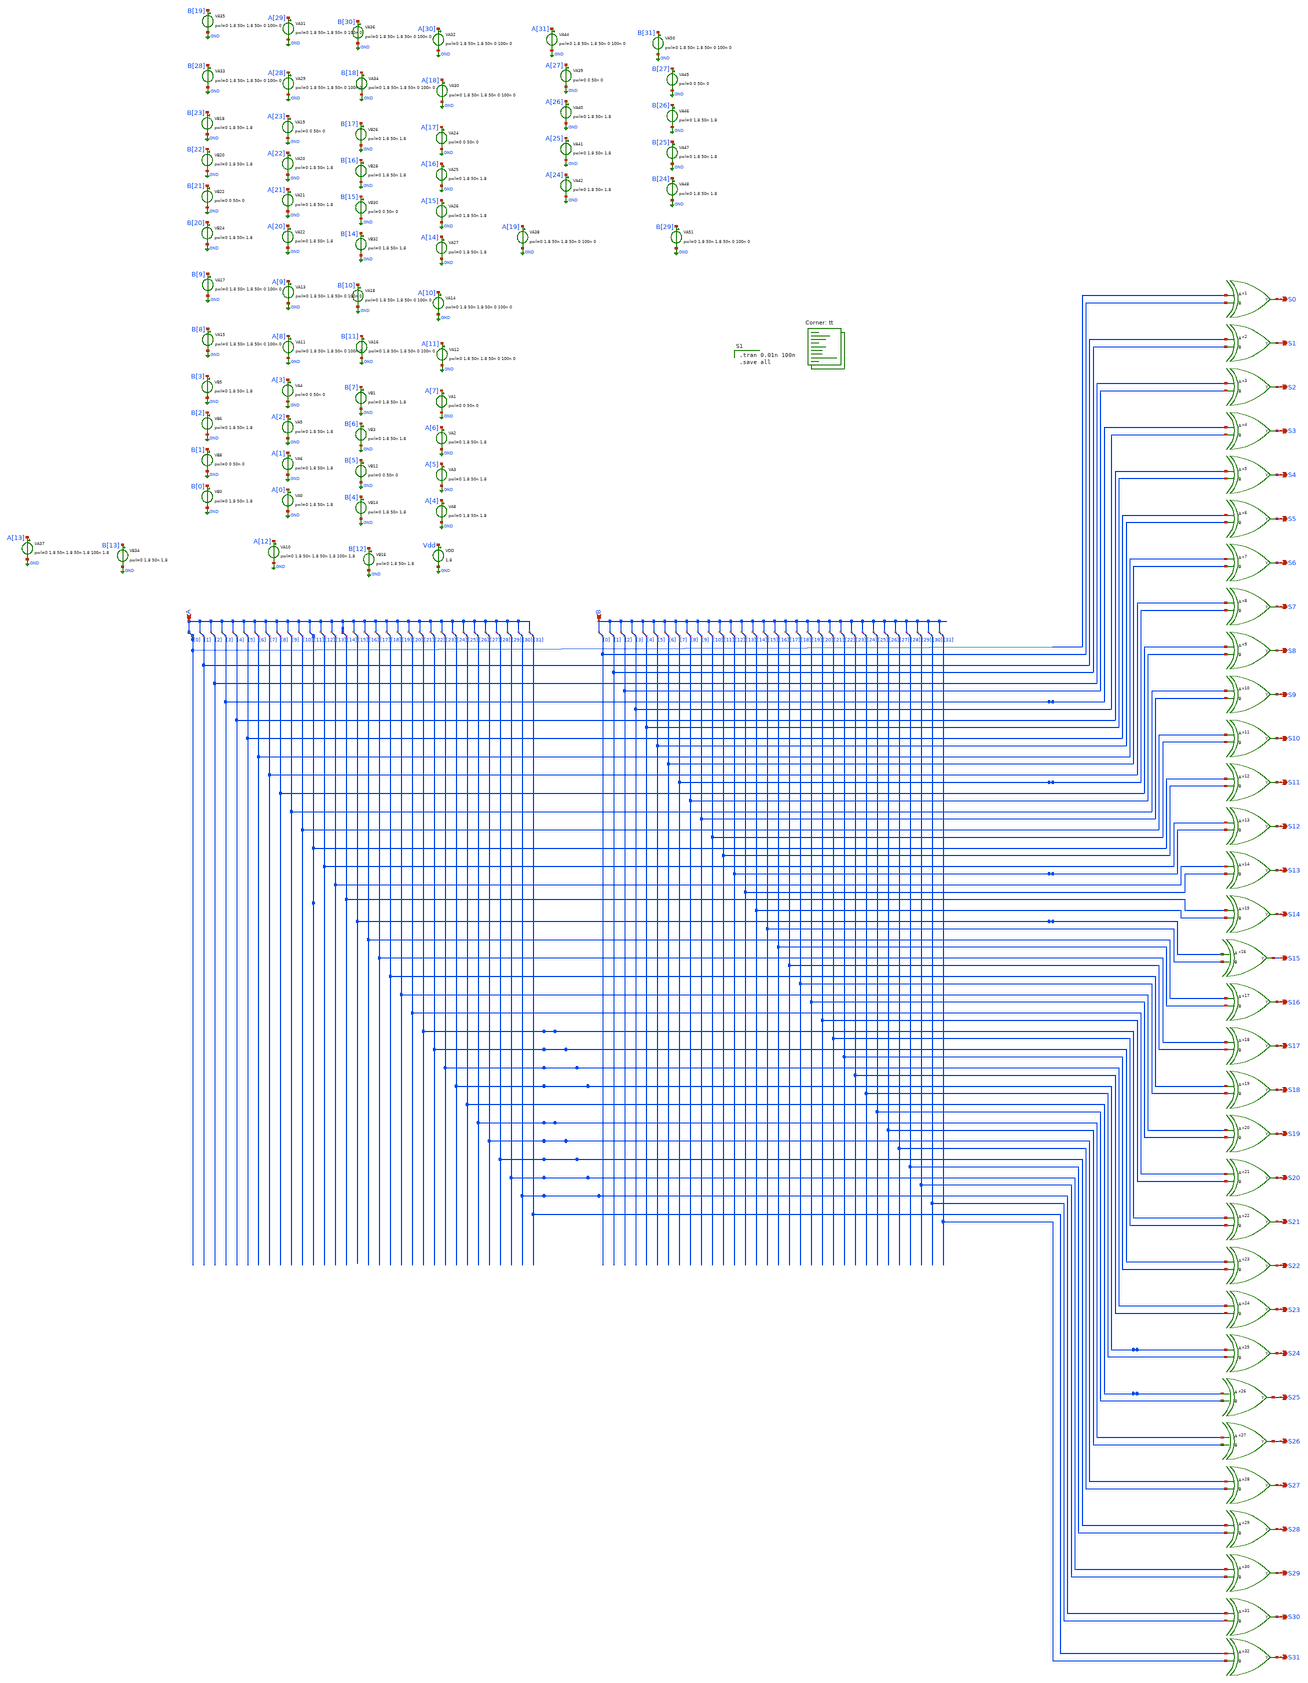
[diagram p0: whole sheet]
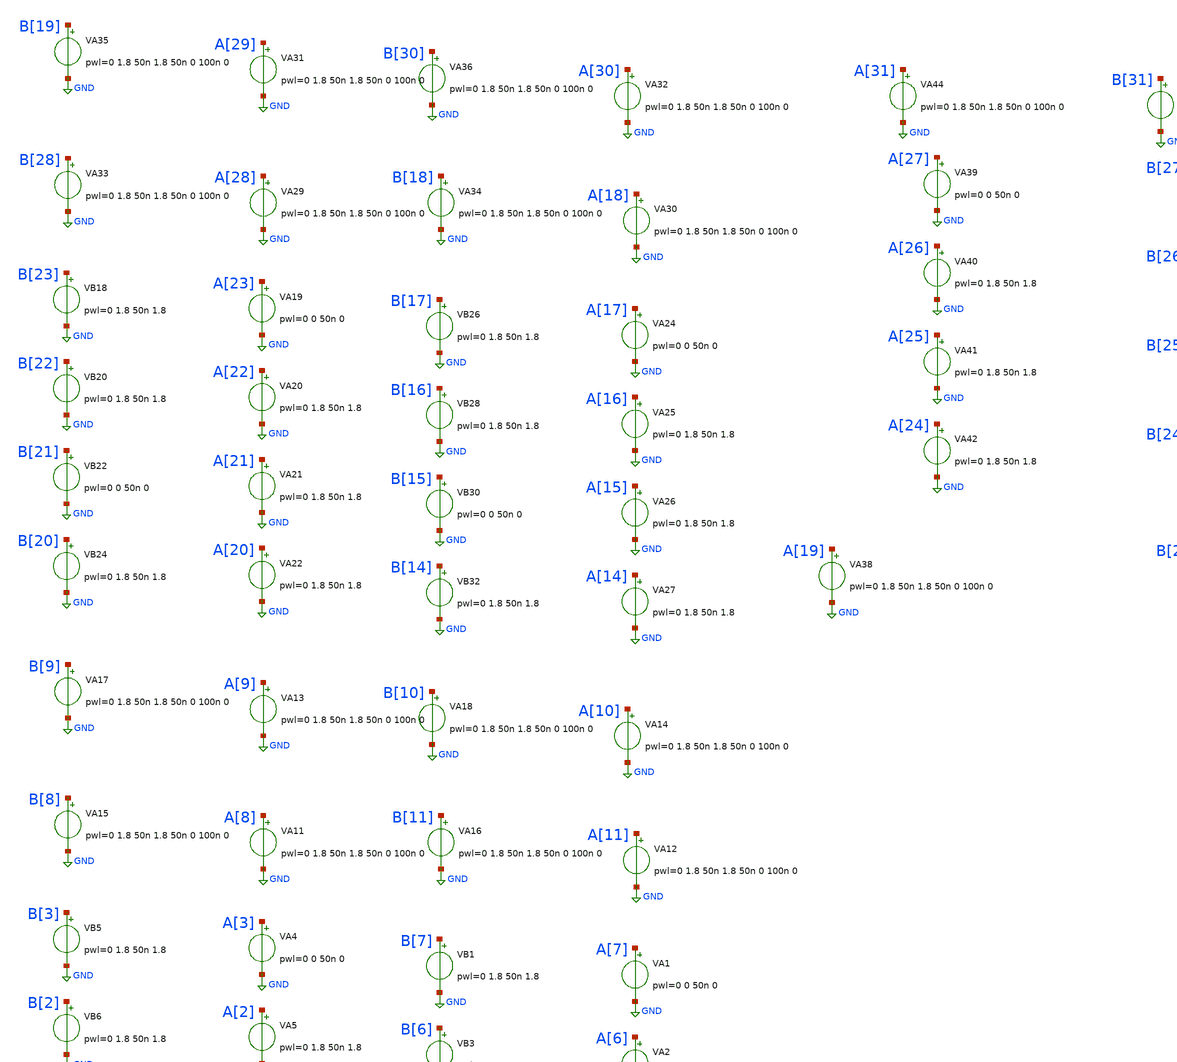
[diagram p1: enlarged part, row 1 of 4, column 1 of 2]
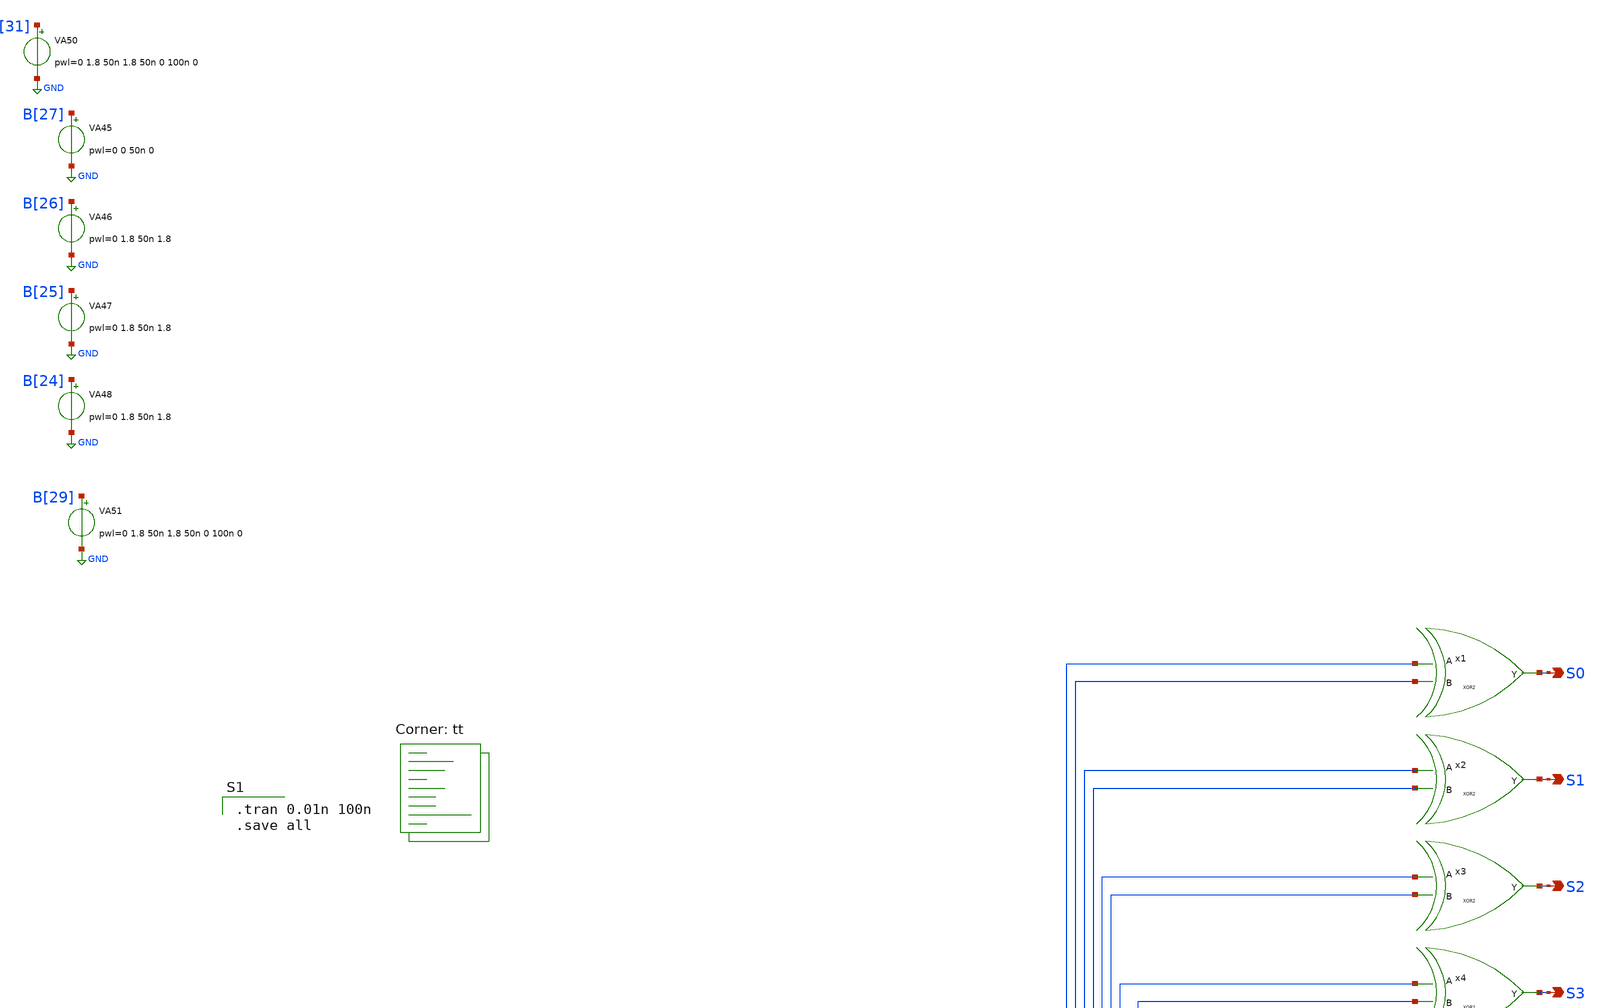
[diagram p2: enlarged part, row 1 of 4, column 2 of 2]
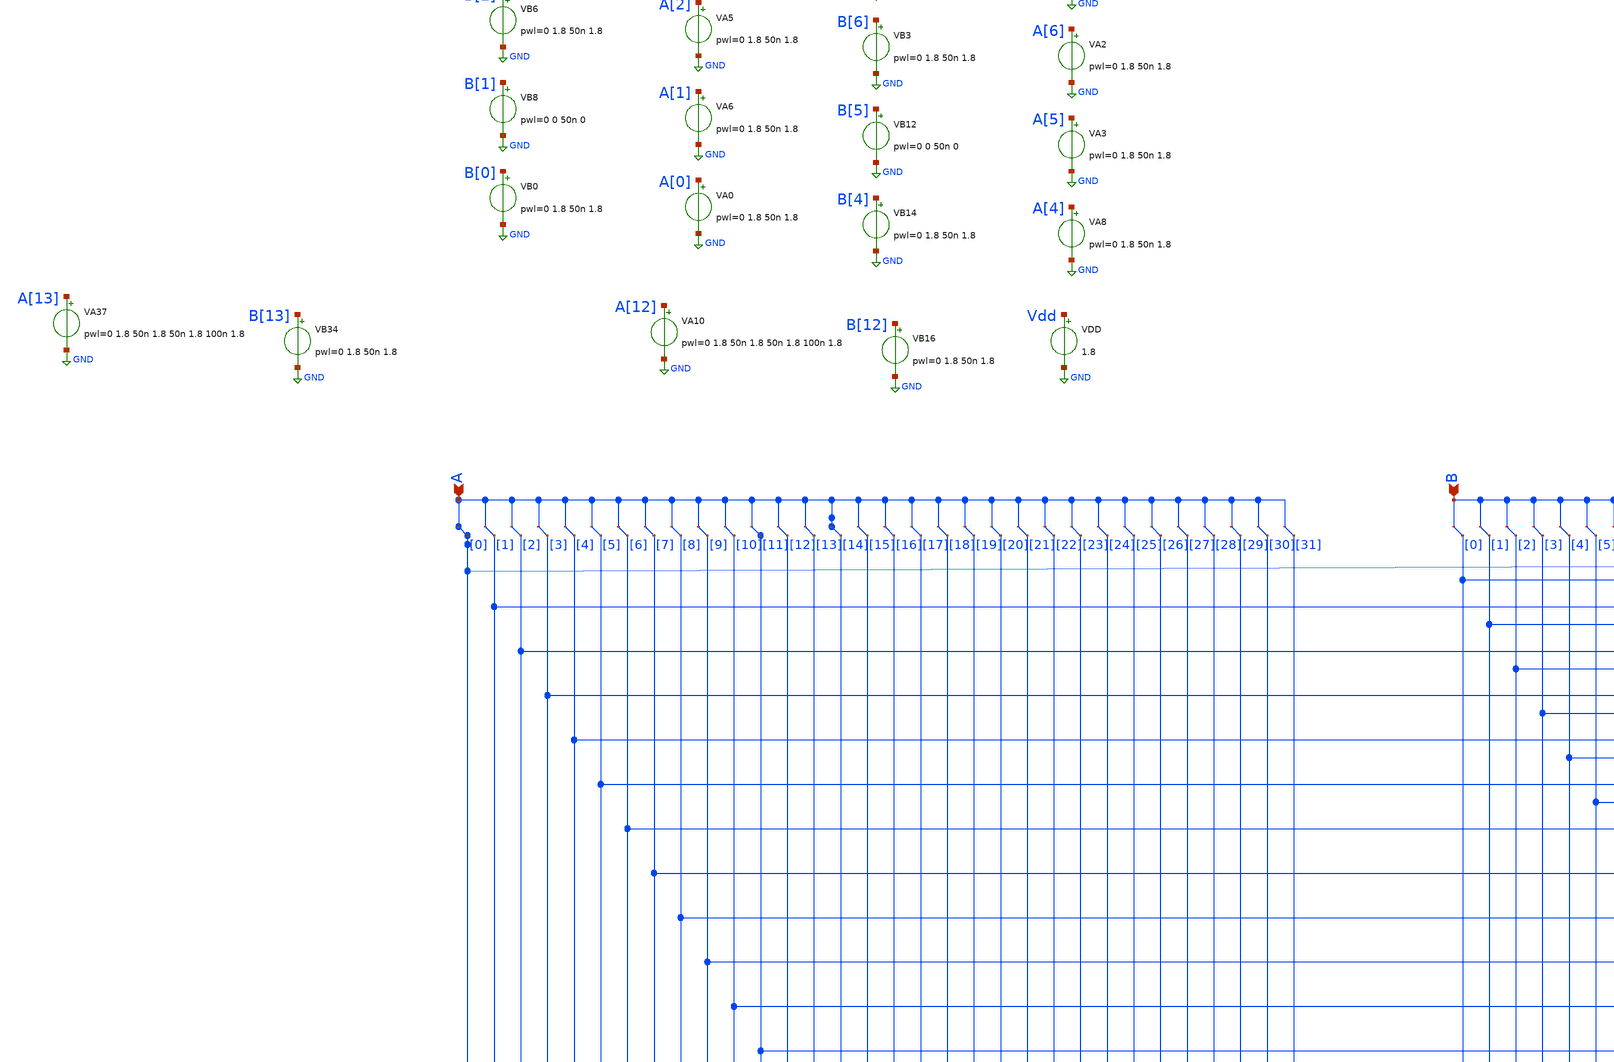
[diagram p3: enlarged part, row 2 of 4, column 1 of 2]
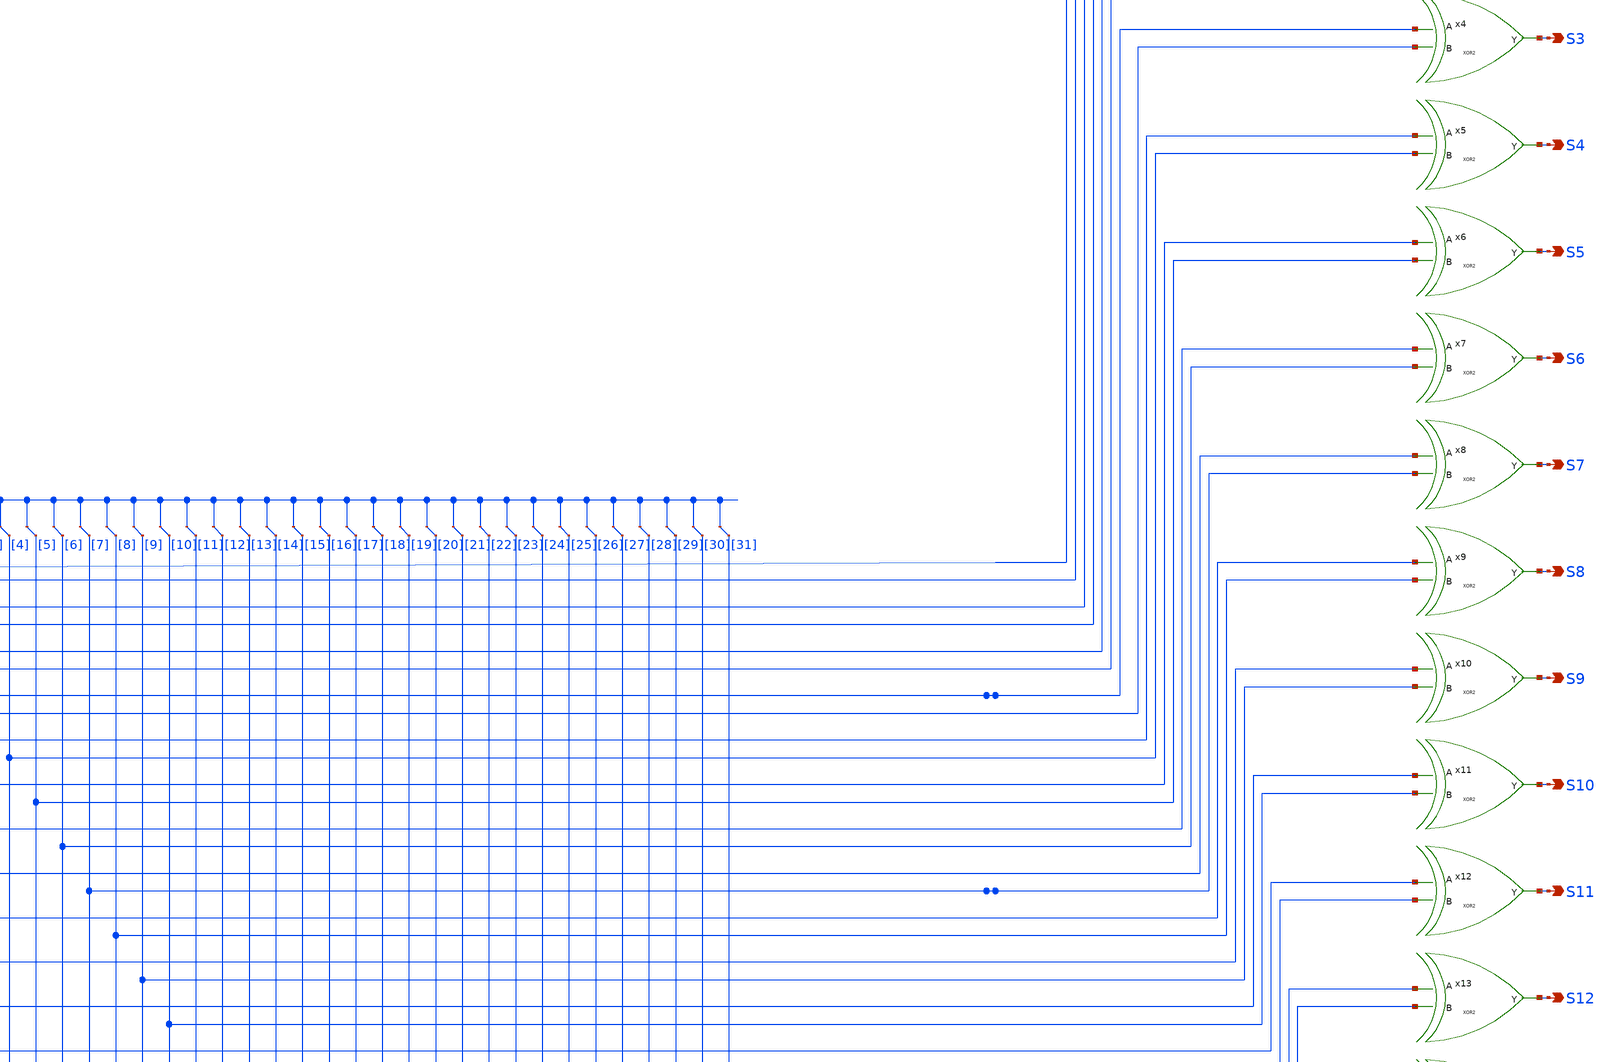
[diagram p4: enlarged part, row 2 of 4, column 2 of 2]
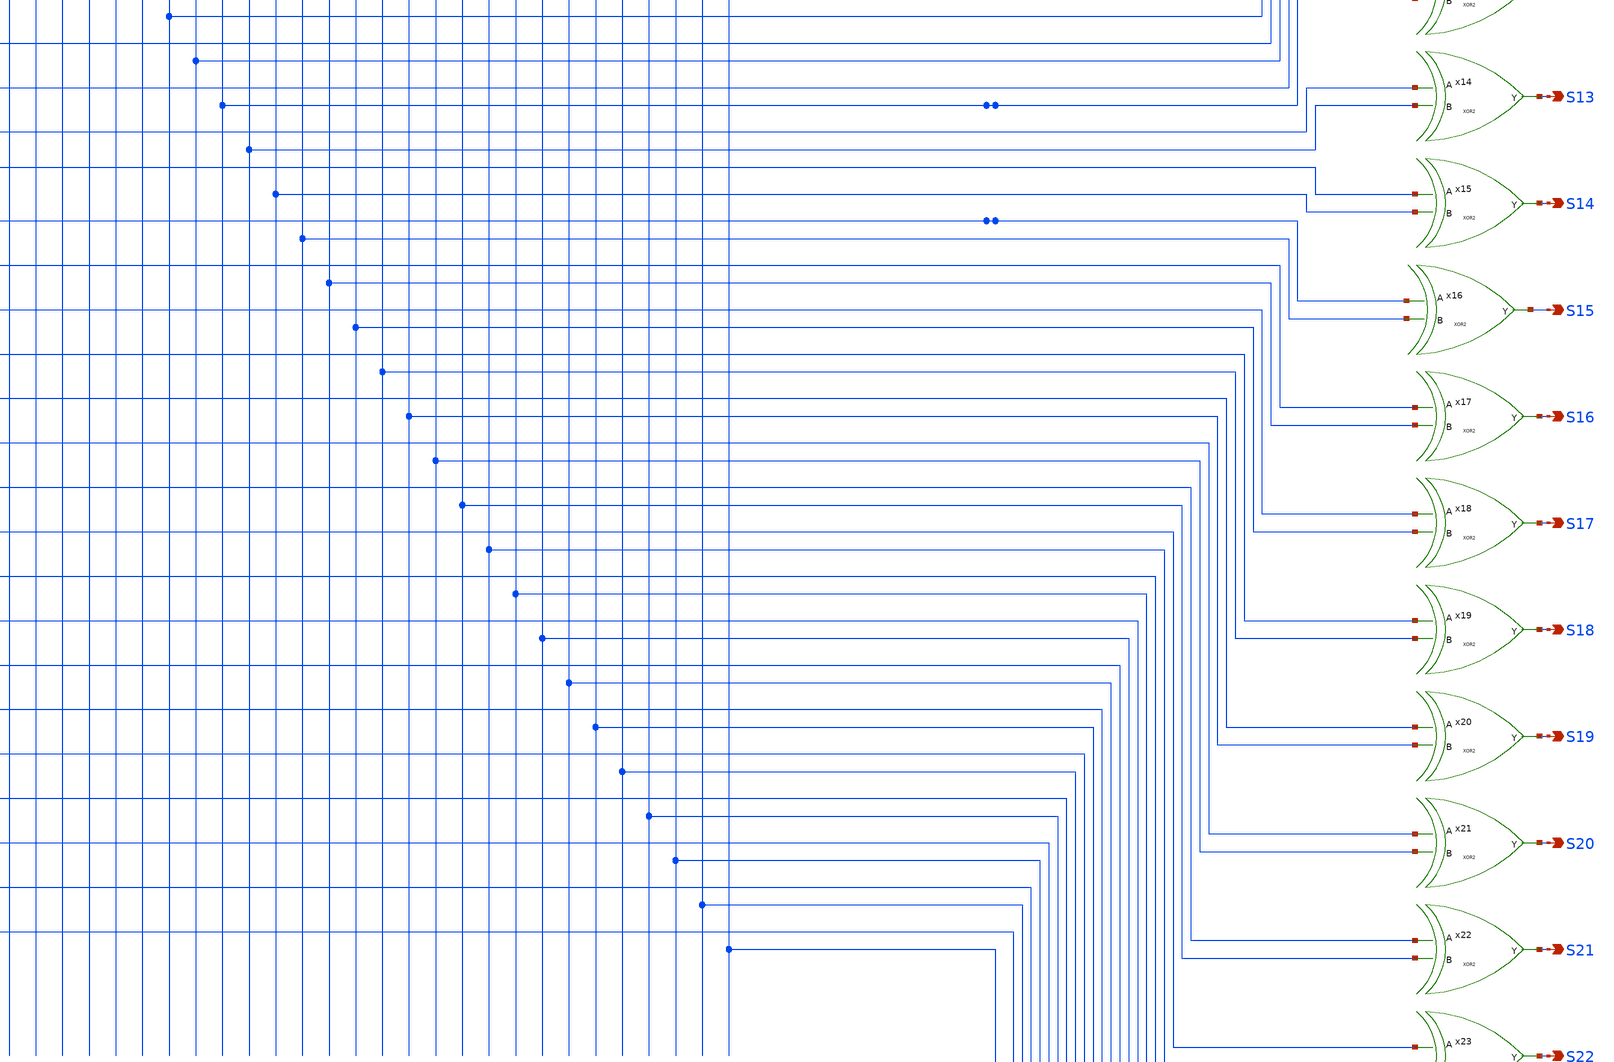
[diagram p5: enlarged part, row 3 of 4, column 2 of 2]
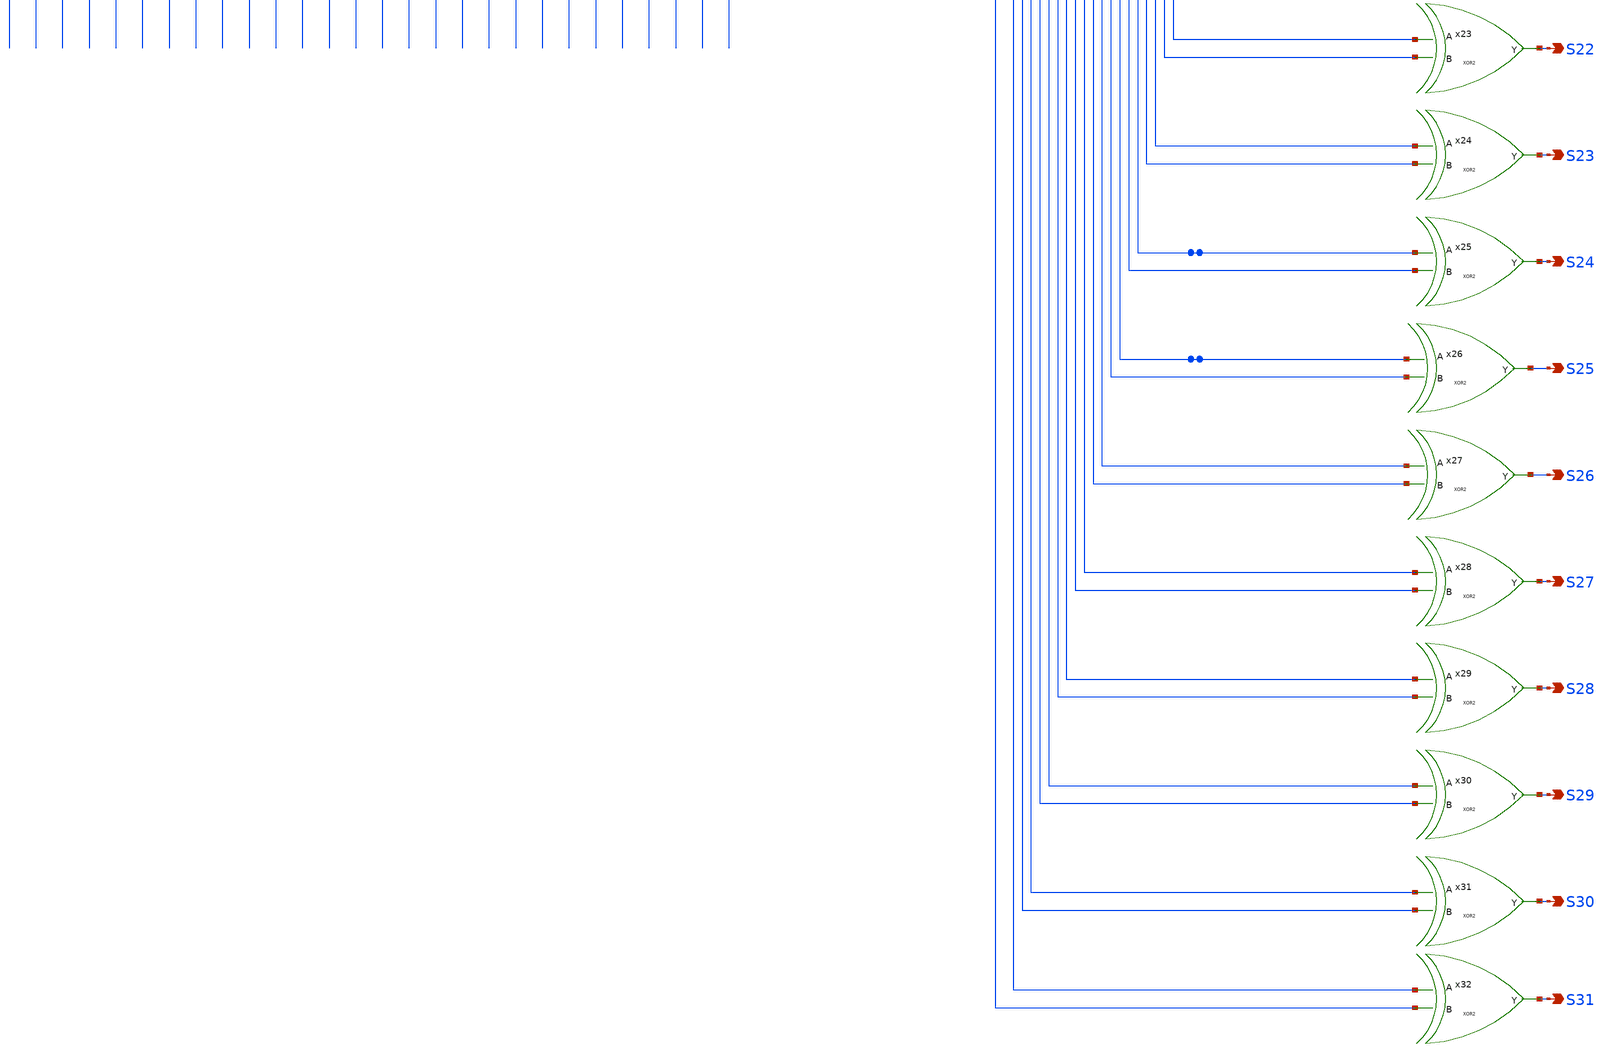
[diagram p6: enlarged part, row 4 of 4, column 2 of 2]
** sch_path: gates/32bit_XORsim.sch
**.subckt 32bit_XORsim S4 S5 S6 S7 S8 S9 S10 S11 S12 S13 S14 S15 S16 S17 S18 S19 S20 S21 S22 S23 S24
*+ S25 S26 S27 S28 S29 S30 S31 S0 S1 S2 S3 A B
*.opin S4
*.opin S5
*.opin S6
*.opin S7
*.opin S8
*.opin S9
*.opin S10
*.opin S11
*.opin S12
*.opin S13
*.opin S14
*.opin S15
*.opin S16
*.opin S17
*.opin S18
*.opin S19
*.opin S20
*.opin S21
*.opin S22
*.opin S23
*.opin S24
*.opin S25
*.opin S26
*.opin S27
*.opin S28
*.opin S29
*.opin S30
*.opin S31
*.opin S0
*.opin S1
*.opin S2
*.opin S3
*.ipin A
*.ipin B
* tap: A --> A[0]
* tap: A --> A[1]
* tap: A --> A[2]
* tap: A --> A[3]
* tap: A --> A[4]
* tap: A --> A[5]
* tap: A --> A[6]
* tap: A --> A[7]
* tap: A --> A[8]
* tap: A --> A[9]
* tap: A --> A[10]
* tap: A --> A[11]
* tap: A --> A[12]
* tap: A --> A[13]
* tap: A --> A[14]
* tap: A --> A[15]
* tap: A --> A[16]
* tap: A --> A[17]
* tap: A --> A[18]
* tap: A --> A[19]
* tap: A --> A[20]
* tap: A --> A[21]
* tap: A --> A[22]
* tap: A --> A[23]
* tap: A --> A[24]
* tap: A --> A[25]
* tap: A --> A[26]
* tap: A --> A[27]
* tap: A --> A[28]
* tap: A --> A[29]
* tap: A --> A[30]
* tap: A --> A[31]
* tap: B --> B[0]
* tap: B --> B[1]
* tap: B --> B[2]
* tap: B --> B[3]
* tap: B --> B[4]
* tap: B --> B[5]
* tap: B --> B[6]
* tap: B --> B[7]
* tap: B --> B[8]
* tap: B --> B[9]
* tap: B --> B[10]
* tap: B --> B[11]
* tap: B --> B[12]
* tap: B --> B[13]
* tap: B --> B[14]
* tap: B --> B[15]
* tap: B --> B[16]
* tap: B --> B[17]
* tap: B --> B[18]
* tap: B --> B[19]
* tap: B --> B[20]
* tap: B --> B[21]
* tap: B --> B[22]
* tap: B --> B[23]
* tap: B --> B[24]
* tap: B --> B[25]
* tap: B --> B[26]
* tap: B --> B[27]
* tap: B --> B[28]
* tap: B --> B[29]
* tap: B --> B[30]
* tap: B --> B[31]
VA10 A[12] GND pwl=0 1.8 50n 1.8 50n 1.8 100n 1.8
VB16 B[12] GND pwl=0 1.8 50n 1.8
VDD Vdd GND 1.8
VA4 A[3] GND pwl=0 0 50n 0
VA5 A[2] GND pwl=0 1.8 50n 1.8
VA6 A[1] GND pwl=0 1.8 50n 1.8
VA0 A[0] GND pwl=0 1.8 50n 1.8
VB5 B[3] GND pwl=0 1.8 50n 1.8
VB6 B[2] GND pwl=0 1.8 50n 1.8
VB8 B[1] GND pwl=0 0 50n 0
VB0 B[0] GND pwl=0 1.8 50n 1.8
VA1 A[7] GND pwl=0 0 50n 0
VA2 A[6] GND pwl=0 1.8 50n 1.8
VA3 A[5] GND pwl=0 1.8 50n 1.8
VA8 A[4] GND pwl=0 1.8 50n 1.8
VB1 B[7] GND pwl=0 1.8 50n 1.8
VB3 B[6] GND pwl=0 1.8 50n 1.8
VB12 B[5] GND pwl=0 0 50n 0
VB14 B[4] GND pwl=0 1.8 50n 1.8
VA11 A[8] GND pwl=0 1.8 50n 1.8 50n 0 100n 0
VA12 A[11] GND pwl=0 1.8 50n 1.8 50n 0 100n 0
VA13 A[9] GND pwl=0 1.8 50n 1.8 50n 0 100n 0
VA14 A[10] GND pwl=0 1.8 50n 1.8 50n 0 100n 0
VA15 B[8] GND pwl=0 1.8 50n 1.8 50n 0 100n 0
VA16 B[11] GND pwl=0 1.8 50n 1.8 50n 0 100n 0
VA17 B[9] GND pwl=0 1.8 50n 1.8 50n 0 100n 0
VA18 B[10] GND pwl=0 1.8 50n 1.8 50n 0 100n 0
VA19 A[23] GND pwl=0 0 50n 0
VA20 A[22] GND pwl=0 1.8 50n 1.8
VA21 A[21] GND pwl=0 1.8 50n 1.8
VA22 A[20] GND pwl=0 1.8 50n 1.8
VB18 B[23] GND pwl=0 1.8 50n 1.8
VB20 B[22] GND pwl=0 1.8 50n 1.8
VB22 B[21] GND pwl=0 0 50n 0
VB24 B[20] GND pwl=0 1.8 50n 1.8
VA24 A[17] GND pwl=0 0 50n 0
VA25 A[16] GND pwl=0 1.8 50n 1.8
VA26 A[15] GND pwl=0 1.8 50n 1.8
VA27 A[14] GND pwl=0 1.8 50n 1.8
VB26 B[17] GND pwl=0 1.8 50n 1.8
VB28 B[16] GND pwl=0 1.8 50n 1.8
VB30 B[15] GND pwl=0 0 50n 0
VB32 B[14] GND pwl=0 1.8 50n 1.8
VA29 A[28] GND pwl=0 1.8 50n 1.8 50n 0 100n 0
VA30 A[18] GND pwl=0 1.8 50n 1.8 50n 0 100n 0
VA31 A[29] GND pwl=0 1.8 50n 1.8 50n 0 100n 0
VA32 A[30] GND pwl=0 1.8 50n 1.8 50n 0 100n 0
VA33 B[28] GND pwl=0 1.8 50n 1.8 50n 0 100n 0
VA34 B[18] GND pwl=0 1.8 50n 1.8 50n 0 100n 0
VA35 B[19] GND pwl=0 1.8 50n 1.8 50n 0 100n 0
VA36 B[30] GND pwl=0 1.8 50n 1.8 50n 0 100n 0
VA37 A[13] GND pwl=0 1.8 50n 1.8 50n 1.8 100n 1.8
VB34 B[13] GND pwl=0 1.8 50n 1.8
VA38 A[19] GND pwl=0 1.8 50n 1.8 50n 0 100n 0
VA39 A[27] GND pwl=0 0 50n 0
VA40 A[26] GND pwl=0 1.8 50n 1.8
VA41 A[25] GND pwl=0 1.8 50n 1.8
VA42 A[24] GND pwl=0 1.8 50n 1.8
VA44 A[31] GND pwl=0 1.8 50n 1.8 50n 0 100n 0
VA45 B[27] GND pwl=0 0 50n 0
VA46 B[26] GND pwl=0 1.8 50n 1.8
VA47 B[25] GND pwl=0 1.8 50n 1.8
VA48 B[24] GND pwl=0 1.8 50n 1.8
VA50 B[31] GND pwl=0 1.8 50n 1.8 50n 0 100n 0
VA51 B[29] GND pwl=0 1.8 50n 1.8 50n 0 100n 0
x1 A[0] B[0] S0 XOR2
x2 A[1] B[1] S1 XOR2
x3 A[2] B[2] S2 XOR2
x4 A[3] B[3] S3 XOR2
x5 A[4] B[4] S4 XOR2
x6 A[5] B[5] S5 XOR2
x7 A[6] B[6] S6 XOR2
x8 A[7] B[7] S7 XOR2
x9 A[8] B[8] S8 XOR2
x10 A[9] B[9] S9 XOR2
x11 A[10] B[10] S10 XOR2
x12 A[11] B[11] S11 XOR2
x13 A[12] B[12] S12 XOR2
x14 A[13] B[13] S13 XOR2
x15 A[14] B[14] S14 XOR2
x16 A[15] B[15] S15 XOR2
x17 A[16] B[16] S16 XOR2
x18 A[17] B[17] S17 XOR2
x19 A[18] B[18] S18 XOR2
x20 A[19] B[19] S19 XOR2
x21 A[20] B[20] S20 XOR2
x22 A[21] B[21] S21 XOR2
x23 A[22] B[22] S22 XOR2
x24 A[23] B[23] S23 XOR2
x25 A[24] B[24] S24 XOR2
x26 A[25] B[25] S25 XOR2
x27 A[26] B[26] S26 XOR2
x28 A[27] B[27] S27 XOR2
x29 A[28] B[28] S28 XOR2
x30 A[29] B[29] S29 XOR2
x31 A[30] B[30] S30 XOR2
x32 A[31] B[31] S31 XOR2
**** begin user architecture code

.tran 0.01n 100n
.save all

.lib $::SKYWATER_MODELS/sky130.lib.spice tt
**** end user architecture code
**.ends

* expanding   symbol:  XOR2.sym # of pins=3
** sym_path: gates/XOR2.sym
** sch_path: gates/XOR2.sch
.subckt XOR2 B A Y
*.ipin A
*.ipin B
*.opin Y
XM1 Y A net5 GND sky130_fd_pr__nfet_01v8 L=0.15 W=1 nf=1 ad='int((nf+1)/2) * W/nf * 0.29' as='int((nf+2)/2) * W/nf * 0.29'
+ pd='2*int((nf+1)/2) * (W/nf + 0.29)' ps='2*int((nf+2)/2) * (W/nf + 0.29)' nrd='0.29 / W' nrs='0.29 / W'
+ sa=0 sb=0 sd=0 mult=1 m=1
XM2 net5 B GND GND sky130_fd_pr__nfet_01v8 L=0.15 W=1 nf=1 ad='int((nf+1)/2) * W/nf * 0.29' as='int((nf+2)/2) * W/nf * 0.29'
+ pd='2*int((nf+1)/2) * (W/nf + 0.29)' ps='2*int((nf+2)/2) * (W/nf + 0.29)' nrd='0.29 / W' nrs='0.29 / W'
+ sa=0 sb=0 sd=0 mult=1 m=1
XM3 Y net1 net2 VDD sky130_fd_pr__pfet_01v8 L=0.15 W=1 nf=1 ad='int((nf+1)/2) * W/nf * 0.29' as='int((nf+2)/2) * W/nf * 0.29'
+ pd='2*int((nf+1)/2) * (W/nf + 0.29)' ps='2*int((nf+2)/2) * (W/nf + 0.29)' nrd='0.29 / W' nrs='0.29 / W'
+ sa=0 sb=0 sd=0 mult=1 m=1
XM4 net2 A VDD VDD sky130_fd_pr__pfet_01v8 L=0.15 W=1 nf=1 ad='int((nf+1)/2) * W/nf * 0.29' as='int((nf+2)/2) * W/nf * 0.29'
+ pd='2*int((nf+1)/2) * (W/nf + 0.29)' ps='2*int((nf+2)/2) * (W/nf + 0.29)' nrd='0.29 / W' nrs='0.29 / W'
+ sa=0 sb=0 sd=0 mult=1 m=1
XM5 net2 B VDD VDD sky130_fd_pr__pfet_01v8 L=0.15 W=1 nf=1 ad='int((nf+1)/2) * W/nf * 0.29' as='int((nf+2)/2) * W/nf * 0.29'
+ pd='2*int((nf+1)/2) * (W/nf + 0.29)' ps='2*int((nf+2)/2) * (W/nf + 0.29)' nrd='0.29 / W' nrs='0.29 / W'
+ sa=0 sb=0 sd=0 mult=1 m=1
XM6 Y net3 net2 VDD sky130_fd_pr__pfet_01v8 L=0.15 W=1 nf=1 ad='int((nf+1)/2) * W/nf * 0.29' as='int((nf+2)/2) * W/nf * 0.29'
+ pd='2*int((nf+1)/2) * (W/nf + 0.29)' ps='2*int((nf+2)/2) * (W/nf + 0.29)' nrd='0.29 / W' nrs='0.29 / W'
+ sa=0 sb=0 sd=0 mult=1 m=1
XM7 Y net1 net4 GND sky130_fd_pr__nfet_01v8 L=0.15 W=1 nf=1 ad='int((nf+1)/2) * W/nf * 0.29' as='int((nf+2)/2) * W/nf * 0.29'
+ pd='2*int((nf+1)/2) * (W/nf + 0.29)' ps='2*int((nf+2)/2) * (W/nf + 0.29)' nrd='0.29 / W' nrs='0.29 / W'
+ sa=0 sb=0 sd=0 mult=1 m=1
XM8 net4 net3 GND GND sky130_fd_pr__nfet_01v8 L=0.15 W=1 nf=1 ad='int((nf+1)/2) * W/nf * 0.29' as='int((nf+2)/2) * W/nf * 0.29'
+ pd='2*int((nf+1)/2) * (W/nf + 0.29)' ps='2*int((nf+2)/2) * (W/nf + 0.29)' nrd='0.29 / W' nrs='0.29 / W'
+ sa=0 sb=0 sd=0 mult=1 m=1
X1 A net1 inv_vtc
X2 B net3 inv_vtc
.ends


* expanding   symbol:  inv_vtc.sym # of pins=2
** sym_path: gates/inv_vtc.sym
** sch_path: gates/inv_vtc.sch
.subckt inv_vtc A Y
*.ipin A
*.opin Y
XM1 Y A VDD VDD sky130_fd_pr__pfet_01v8 L=0.15 W=2 nf=1 ad='int((nf+1)/2) * W/nf * 0.29' as='int((nf+2)/2) * W/nf * 0.29'
+ pd='2*int((nf+1)/2) * (W/nf + 0.29)' ps='2*int((nf+2)/2) * (W/nf + 0.29)' nrd='0.29 / W' nrs='0.29 / W'
+ sa=0 sb=0 sd=0 mult=1 m=1
XM2 Y A GND GND sky130_fd_pr__nfet_01v8 L=0.15 W=1 nf=1 ad='int((nf+1)/2) * W/nf * 0.29' as='int((nf+2)/2) * W/nf * 0.29'
+ pd='2*int((nf+1)/2) * (W/nf + 0.29)' ps='2*int((nf+2)/2) * (W/nf + 0.29)' nrd='0.29 / W' nrs='0.29 / W'
+ sa=0 sb=0 sd=0 mult=1 m=1
.ends

.GLOBAL GND
.GLOBAL VDD
.end
